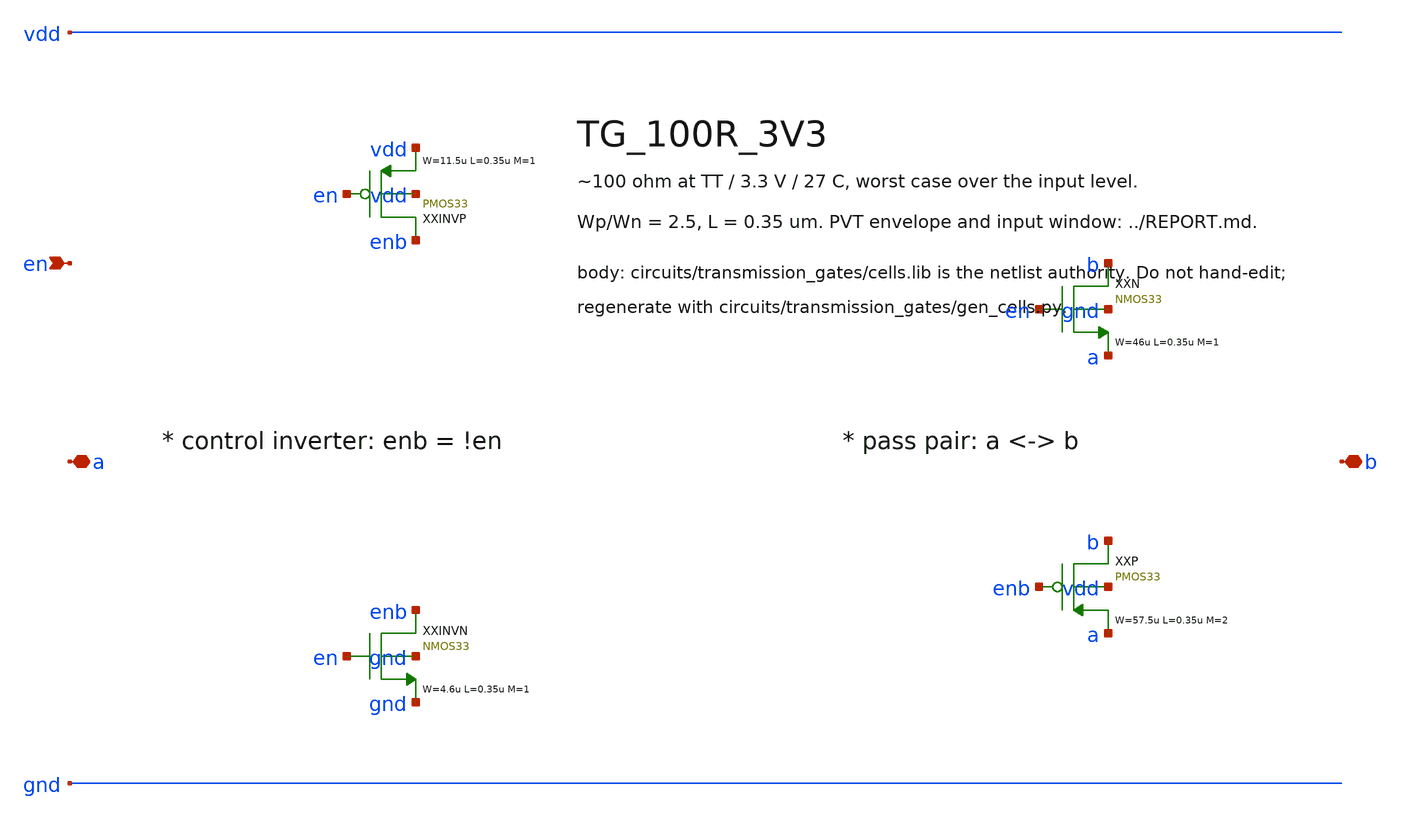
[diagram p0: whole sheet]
** sch_path: xschem/transmission_gates/TG_100R_3V3.sch
**.subckt TG_100R_3V3 a b en
*.iopin a
*.iopin b
*.ipin en
XXINVP enb en vdd vdd PMOS33 W=11.5u L=0.35u M=1 MM_SIGMA=0
XXINVN enb en gnd gnd NMOS33 W=4.6u L=0.35u M=1 MM_SIGMA=0
XXN b en a gnd NMOS33 W=46u L=0.35u M=1 MM_SIGMA=0
XXP b enb a vdd PMOS33 W=57.5u L=0.35u M=2 MM_SIGMA=0
**.ends
.end
